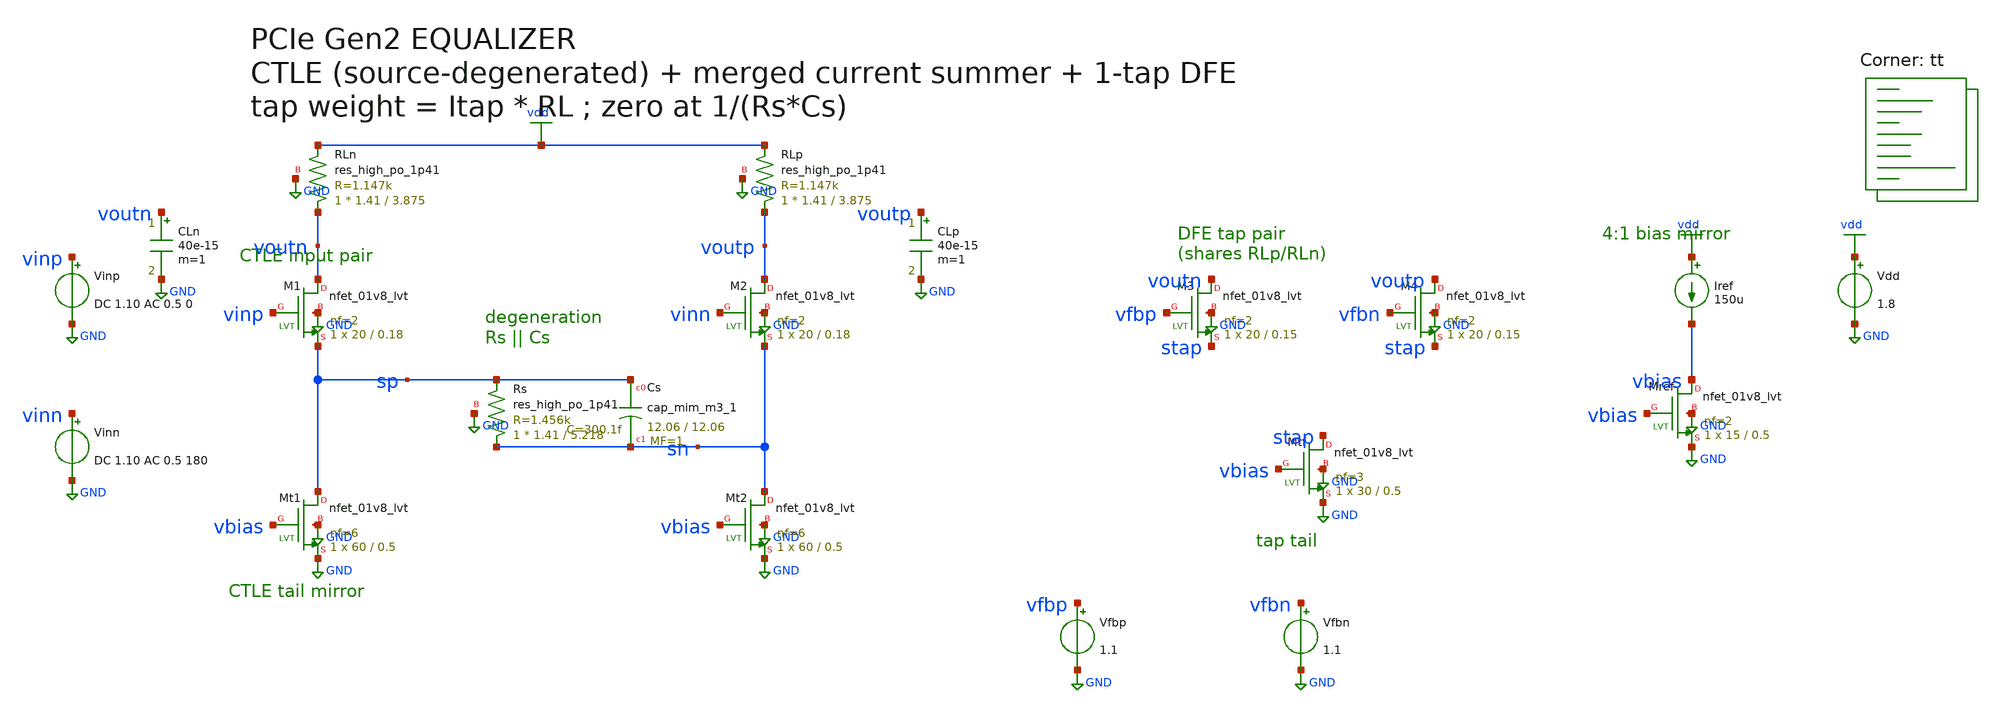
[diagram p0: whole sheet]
** sch_path: netlists/eq_tb.sch
**.subckt eq_tb
XM1 voutn vinp sp GND sky130_fd_pr__nfet_01v8_lvt L=0.18 W=20 nf=2 ad=0 as=0 pd=0 ps=0 nrd=0 nrs=0
+ sa=0 sb=0 sd=0 mult=1 m=1
XM2 voutp vinn sn GND sky130_fd_pr__nfet_01v8_lvt L=0.18 W=20 nf=2 ad=0 as=0 pd=0 ps=0 nrd=0 nrs=0
+ sa=0 sb=0 sd=0 mult=1 m=1
XRLn voutn vdd GND sky130_fd_pr__res_high_po_1p41 L=3.875 mult=1 m=1
XRLp voutp vdd GND sky130_fd_pr__res_high_po_1p41 L=3.875 mult=1 m=1
XRs sn sp GND sky130_fd_pr__res_high_po_1p41 L=5.218 mult=1 m=1
XCs sp sn sky130_fd_pr__cap_mim_m3_1 W=12.06 L=12.06 MF=1 m=1
CLn voutn GND 40e-15 m=1
CLp voutp GND 40e-15 m=1
XMt1 sp vbias GND GND sky130_fd_pr__nfet_01v8_lvt L=0.5 W=60 nf=6 ad=0 as=0 pd=0 ps=0 nrd=0 nrs=0
+ sa=0 sb=0 sd=0 mult=1 m=1
XMt2 sn vbias GND GND sky130_fd_pr__nfet_01v8_lvt L=0.5 W=60 nf=6 ad=0 as=0 pd=0 ps=0 nrd=0 nrs=0
+ sa=0 sb=0 sd=0 mult=1 m=1
XM3 voutn vfbp stap GND sky130_fd_pr__nfet_01v8_lvt L=0.15 W=20 nf=2 ad=0 as=0 pd=0 ps=0 nrd=0 nrs=0
+ sa=0 sb=0 sd=0 mult=1 m=1
XM4 voutp vfbn stap GND sky130_fd_pr__nfet_01v8_lvt L=0.15 W=20 nf=2 ad=0 as=0 pd=0 ps=0 nrd=0 nrs=0
+ sa=0 sb=0 sd=0 mult=1 m=1
XMtf stap vbias GND GND sky130_fd_pr__nfet_01v8_lvt L=0.5 W=30 nf=3 ad=0 as=0 pd=0 ps=0 nrd=0 nrs=0
+ sa=0 sb=0 sd=0 mult=1 m=1
XMref vbias vbias GND GND sky130_fd_pr__nfet_01v8_lvt L=0.5 W=15 nf=2 ad=0 as=0 pd=0 ps=0 nrd=0
+ nrs=0 sa=0 sb=0 sd=0 mult=1 m=1
Iref vdd vbias 150u
Vdd vdd GND 1.8
Vinp vinp GND DC 1.10 AC 0.5 0
Vinn vinn GND DC 1.10 AC 0.5 180
Vfbp vfbp GND 1.1
Vfbn vfbn GND 1.1
**** begin user architecture code
.lib $::SKYWATER_MODELS/sky130.lib.spice tt
**** end user architecture code
**.ends
.GLOBAL vdd
.GLOBAL GND
**** begin user architecture code

.control
save all
op
echo ---------- BIAS: want vds > vdsat on BOTH ----------
print @m.xm1.msky130_fd_pr__nfet_01v8_lvt[id]
print @m.xm1.msky130_fd_pr__nfet_01v8_lvt[vds]
print @m.xm1.msky130_fd_pr__nfet_01v8_lvt[vdsat]
print @m.xmt1.msky130_fd_pr__nfet_01v8_lvt[vds]
print @m.xmt1.msky130_fd_pr__nfet_01v8_lvt[vdsat]
print i(Vdd)
ac dec 40 1e6 20e9
let g = vdb(voutp,voutn)
echo ---------- AC: expect peaking ~9.0 dB, f_peak ~2.52 GHz ----------
print g[0]
print maximum(g)
plot g
.endc


**** end user architecture code
.end
